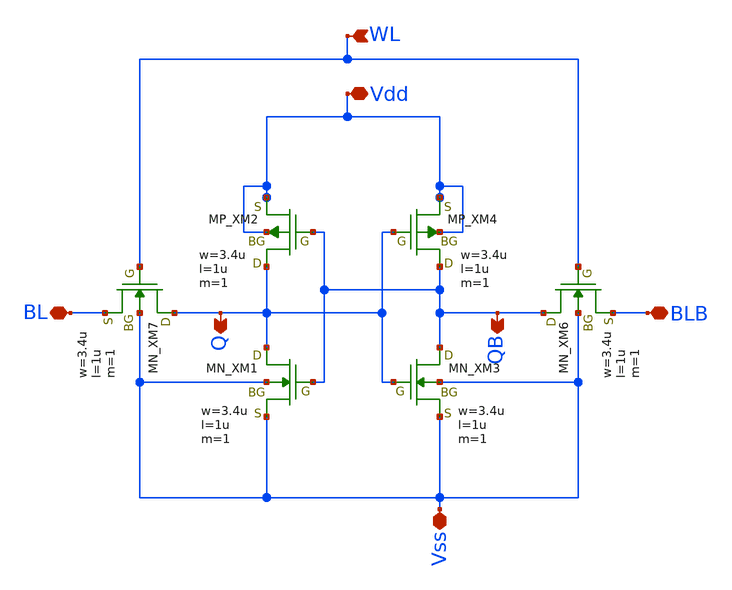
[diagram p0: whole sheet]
** sch_path: member_project/SRAM/PenguinEino/learning/schematics/sram_dense.sch
**.subckt sram_dense Vdd BLB BL WL Q QB Vss
*.iopin Vdd
*.iopin BLB
*.iopin BL
*.ipin WL
*.opin Q
*.opin QB
*.iopin Vss
XXM1 Q QB Vss Vss NMOS w=3.4u l=1u nrd=0 nrs=0 m=1
XXM2 Q QB Vdd Vdd PMOS w=3.4u l=1u nrd=0 nrs=0 m=1
XXM3 QB Q Vss Vss NMOS w=3.4u l=1u nrd=0 nrs=0 m=1
XXM4 QB Q Vdd Vdd PMOS w=3.4u l=1u nrd=0 nrs=0 m=1
XXM7 Q WL BL Vss NMOS w=3.4u l=1u nrd=0 nrs=0 m=1
XXM6 QB WL BLB Vss NMOS w=3.4u l=1u nrd=0 nrs=0 m=1
**.ends
.end
